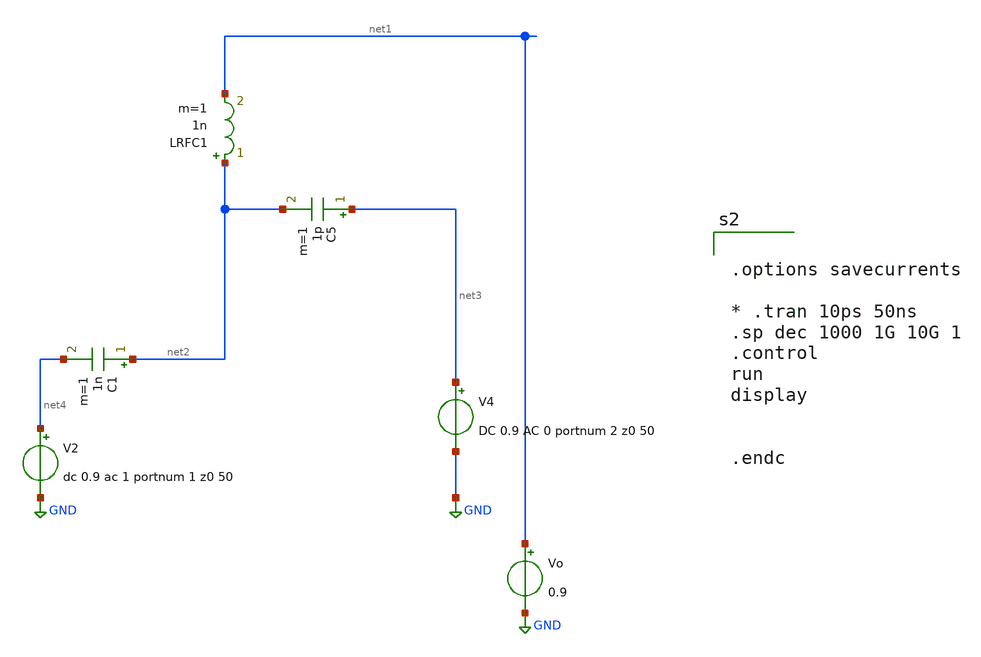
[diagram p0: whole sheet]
** sch_path: xschem/sptest_1.sch
**.subckt sptest_1
Vo net1 GND 0.9
LRFC1 net2 net1 1n m=1
C5 net3 net2 1p m=1
V2 net4 GND dc 0.9 ac 1 portnum 1 z0 50
C1 net2 net4 1n m=1
V4 net3 GND DC 0.9 AC 0 portnum 2 z0 50
**** begin user architecture code
.lib $::SKYWATER_MODELS/sky130.lib.spice tt
* .include $::PDKPATH/libs.ref/sky130_fd_sc_hvl/spice/sky130_fd_sc_hvl.spice



.options savecurrents

* .tran 10ps 50ns
.sp dec 1000 1G 10G 1
.control
run
display


.endc


**** end user architecture code
**.ends
.GLOBAL GND
.end
